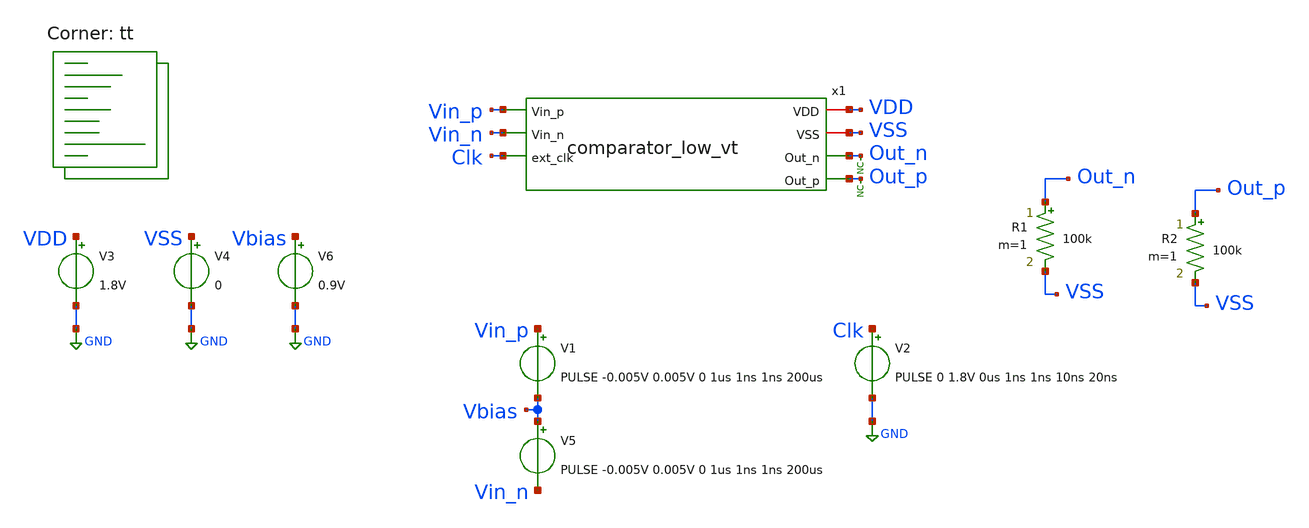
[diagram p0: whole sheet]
** sch_path: xschem/tests/comparator/comparator_fast_low_vt_small_v_test.sch
**.subckt comparator_fast_low_vt_small_v_test
V3 VDD GND 1.8V
V4 VSS GND 0
V1 Vin_p Vbias PULSE -0.005V 0.005V 0 1us 1ns 1ns 200us
V2 Clk GND PULSE 0 1.8V 0us 1ns 1ns 10ns 20ns
* noconn Out_p
* noconn Out_n
V5 Vbias Vin_n PULSE -0.005V 0.005V 0 1us 1ns 1ns 200us
V6 Vbias GND 0.9V
R1 Out_n VSS 100k m=1
R2 Out_p VSS 100k m=1
x1 VDD VSS Vin_p Out_n Vin_n Clk Out_p comparator_low_vt
**** begin user architecture code
 *.lib $::SKYWATER_MODELS/sky130.lib.spice tt
.include $::SKYWATER_STDCELLS/sky130_fd_sc_hd.spice


.options acct list
.temp 25
.control
save all
tran 0.1n 1u
*dc V1 0 1.8V 0.1
plot Vin_p-Vin_n Out_p-Out_n Clk-4
plot Vin_p-Vin_n x1.pre_amp_p-x1.pre_amp_n Clk-4
plot Vin_p-Vin_n x1.pre_amp_p-x1.pre_amp_n
plot x1.pre_amp_p x1.pre_amp_n
*write comparator_fast_test.raw
.endc


.lib $::SKYWATER_MODELS/sky130.lib.spice tt
**** end user architecture code
**.ends

* expanding   symbol:  src/comparator/comparator_low_vt.sym # of pins=7
** sym_path: xschem/src/comparator/comparator_low_vt.sym
** sch_path: xschem/src/comparator/comparator_low_vt.sch
.subckt comparator_low_vt VDD VSS Vin_p Out_n Vin_n ext_clk Out_p
*.iopin VDD
*.iopin VSS
*.ipin Vin_p
*.opin Out_n
*.ipin Vin_n
*.opin Out_p
*.ipin ext_clk
XM1 Pre_Amp_p Clk_n VDD VDD sky130_fd_pr__pfet_01v8 L=0.15 W=20 nf=1 ad='int((nf+1)/2) * W/nf * 0.29'
+ as='int((nf+2)/2) * W/nf * 0.29' pd='2*int((nf+1)/2) * (W/nf + 0.29)' ps='2*int((nf+2)/2) * (W/nf + 0.29)'
+ nrd='0.29 / W' nrs='0.29 / W' sa=0 sb=0 sd=0 mult=1 m=1
XM2 Pre_Amp_n Clk_n VDD VDD sky130_fd_pr__pfet_01v8 L=0.15 W=20 nf=1 ad='int((nf+1)/2) * W/nf * 0.29'
+ as='int((nf+2)/2) * W/nf * 0.29' pd='2*int((nf+1)/2) * (W/nf + 0.29)' ps='2*int((nf+2)/2) * (W/nf + 0.29)'
+ nrd='0.29 / W' nrs='0.29 / W' sa=0 sb=0 sd=0 mult=1 m=1
XM5 net3 net5 VDD VDD sky130_fd_pr__pfet_01v8 L=0.15 W=1.605 nf=1 ad='int((nf+1)/2) * W/nf * 0.29' as='int((nf+2)/2) * W/nf * 0.29'
+ pd='2*int((nf+1)/2) * (W/nf + 0.29)' ps='2*int((nf+2)/2) * (W/nf + 0.29)' nrd='0.29 / W' nrs='0.29 / W'
+ sa=0 sb=0 sd=0 mult=4 m=4
XM6 net2 net4 VDD VDD sky130_fd_pr__pfet_01v8 L=0.15 W=1.605 nf=1 ad='int((nf+1)/2) * W/nf * 0.29' as='int((nf+2)/2) * W/nf * 0.29'
+ pd='2*int((nf+1)/2) * (W/nf + 0.29)' ps='2*int((nf+2)/2) * (W/nf + 0.29)' nrd='0.29 / W' nrs='0.29 / W'
+ sa=0 sb=0 sd=0 mult=4 m=4
XM9 net1 Clk VSS VSS sky130_fd_pr__nfet_01v8 L=0.15 W=50 nf=1 ad='int((nf+1)/2) * W/nf * 0.29' as='int((nf+2)/2) * W/nf * 0.29'
+ pd='2*int((nf+1)/2) * (W/nf + 0.29)' ps='2*int((nf+2)/2) * (W/nf + 0.29)' nrd='0.29 / W' nrs='0.29 / W'
+ sa=0 sb=0 sd=0 mult=1 m=1
XM11 net4 Clk_latch_n VSS VSS sky130_fd_pr__nfet_01v8 L=0.15 W=0.91 nf=1 ad='int((nf+1)/2) * W/nf * 0.29'
+ as='int((nf+2)/2) * W/nf * 0.29' pd='2*int((nf+1)/2) * (W/nf + 0.29)' ps='2*int((nf+2)/2) * (W/nf + 0.29)'
+ nrd='0.29 / W' nrs='0.29 / W' sa=0 sb=0 sd=0 mult=4 m=4
XM12 net4 net5 VSS VSS sky130_fd_pr__nfet_01v8 L=0.15 W=0.91 nf=1 ad='int((nf+1)/2) * W/nf * 0.29' as='int((nf+2)/2) * W/nf * 0.29'
+ pd='2*int((nf+1)/2) * (W/nf + 0.29)' ps='2*int((nf+2)/2) * (W/nf + 0.29)' nrd='0.29 / W' nrs='0.29 / W'
+ sa=0 sb=0 sd=0 mult=4 m=4
XM13 net5 net4 VSS VSS sky130_fd_pr__nfet_01v8 L=0.15 W=0.91 nf=1 ad='int((nf+1)/2) * W/nf * 0.29' as='int((nf+2)/2) * W/nf * 0.29'
+ pd='2*int((nf+1)/2) * (W/nf + 0.29)' ps='2*int((nf+2)/2) * (W/nf + 0.29)' nrd='0.29 / W' nrs='0.29 / W'
+ sa=0 sb=0 sd=0 mult=4 m=4
XM14 net5 Clk_latch_n VSS VSS sky130_fd_pr__nfet_01v8 L=0.15 W=0.91 nf=1 ad='int((nf+1)/2) * W/nf * 0.29'
+ as='int((nf+2)/2) * W/nf * 0.29' pd='2*int((nf+1)/2) * (W/nf + 0.29)' ps='2*int((nf+2)/2) * (W/nf + 0.29)'
+ nrd='0.29 / W' nrs='0.29 / W' sa=0 sb=0 sd=0 mult=4 m=4
XM7 net5 Pre_Amp_n net2 VDD sky130_fd_pr__pfet_01v8 L=0.15 W=1.605 nf=1 ad='int((nf+1)/2) * W/nf * 0.29'
+ as='int((nf+2)/2) * W/nf * 0.29' pd='2*int((nf+1)/2) * (W/nf + 0.29)' ps='2*int((nf+2)/2) * (W/nf + 0.29)'
+ nrd='0.29 / W' nrs='0.29 / W' sa=0 sb=0 sd=0 mult=8 m=8
XM8 net4 Pre_Amp_p net3 VDD sky130_fd_pr__pfet_01v8 L=0.15 W=1.605 nf=1 ad='int((nf+1)/2) * W/nf * 0.29'
+ as='int((nf+2)/2) * W/nf * 0.29' pd='2*int((nf+1)/2) * (W/nf + 0.29)' ps='2*int((nf+2)/2) * (W/nf + 0.29)'
+ nrd='0.29 / W' nrs='0.29 / W' sa=0 sb=0 sd=0 mult=8 m=8
XC1 Pre_Amp_p VSS sky130_fd_pr__cap_mim_m3_1 W=1 L=1 MF=1 m=1
XC2 Pre_Amp_n VSS sky130_fd_pr__cap_mim_m3_1 W=1 L=1 MF=1 m=1
x1 net4 VSS VSS VDD VDD net6 sky130_fd_sc_hd__buf_1
x2 net6 VSS VSS VDD VDD net7 sky130_fd_sc_hd__buf_4
x3 net7 VSS VSS VDD VDD Out_n sky130_fd_sc_hd__buf_8
x4 net5 VSS VSS VDD VDD net8 sky130_fd_sc_hd__buf_1
x5 net8 VSS VSS VDD VDD net9 sky130_fd_sc_hd__buf_4
x6 net9 VSS VSS VDD VDD Out_p sky130_fd_sc_hd__buf_8
XC3 net5 VSS sky130_fd_pr__cap_mim_m3_1 W=1 L=1 MF=1 m=1
XC4 net4 VSS sky130_fd_pr__cap_mim_m3_1 W=1 L=1 MF=1 m=1
x7 ext_clk VSS VSS VDD VDD net10 sky130_fd_sc_hd__buf_1
x8 Clk_n VSS VSS VDD VDD net14 sky130_fd_sc_hd__clkdlybuf4s15_1
x9 net11 VSS VSS VDD VDD Clk_latch_n sky130_fd_sc_hd__buf_2
x10 net14 VSS VSS VDD VDD net15 sky130_fd_sc_hd__clkdlybuf4s15_1
x11 net15 VSS VSS VDD VDD net11 sky130_fd_sc_hd__clkdlybuf4s50_1
x13 Clk VSS VSS VDD VDD net12 sky130_fd_sc_hd__inv_2
x12 net10 VSS VSS VDD VDD net13 sky130_fd_sc_hd__buf_2
x14 net13 VSS VSS VDD VDD net16 sky130_fd_sc_hd__buf_4
x15 net16 VSS VSS VDD VDD Clk sky130_fd_sc_hd__buf_8
XC5 Clk VSS sky130_fd_pr__cap_mim_m3_1 W=3 L=3 MF=1 m=1
XC6 Clk_n VSS sky130_fd_pr__cap_mim_m3_1 W=1 L=1 MF=1 m=1
XC7 Clk_latch_n VSS sky130_fd_pr__cap_mim_m3_1 W=1 L=1 MF=1 m=1
x16 net12 VSS VSS VDD VDD Clk_n sky130_fd_sc_hd__buf_4
XM10 Pre_Amp_n Vin_p net1 VSS sky130_fd_pr__nfet_01v8_lvt L=0.15 W=40 nf=1 ad='int((nf+1)/2) * W/nf * 0.29'
+ as='int((nf+2)/2) * W/nf * 0.29' pd='2*int((nf+1)/2) * (W/nf + 0.29)' ps='2*int((nf+2)/2) * (W/nf + 0.29)'
+ nrd='0.29 / W' nrs='0.29 / W' sa=0 sb=0 sd=0 mult=1 m=1
XM3 Pre_Amp_p Vin_n net1 VSS sky130_fd_pr__nfet_01v8_lvt L=0.15 W=40 nf=1 ad='int((nf+1)/2) * W/nf * 0.29'
+ as='int((nf+2)/2) * W/nf * 0.29' pd='2*int((nf+1)/2) * (W/nf + 0.29)' ps='2*int((nf+2)/2) * (W/nf + 0.29)'
+ nrd='0.29 / W' nrs='0.29 / W' sa=0 sb=0 sd=0 mult=1 m=1
.ends

.GLOBAL GND
.end
